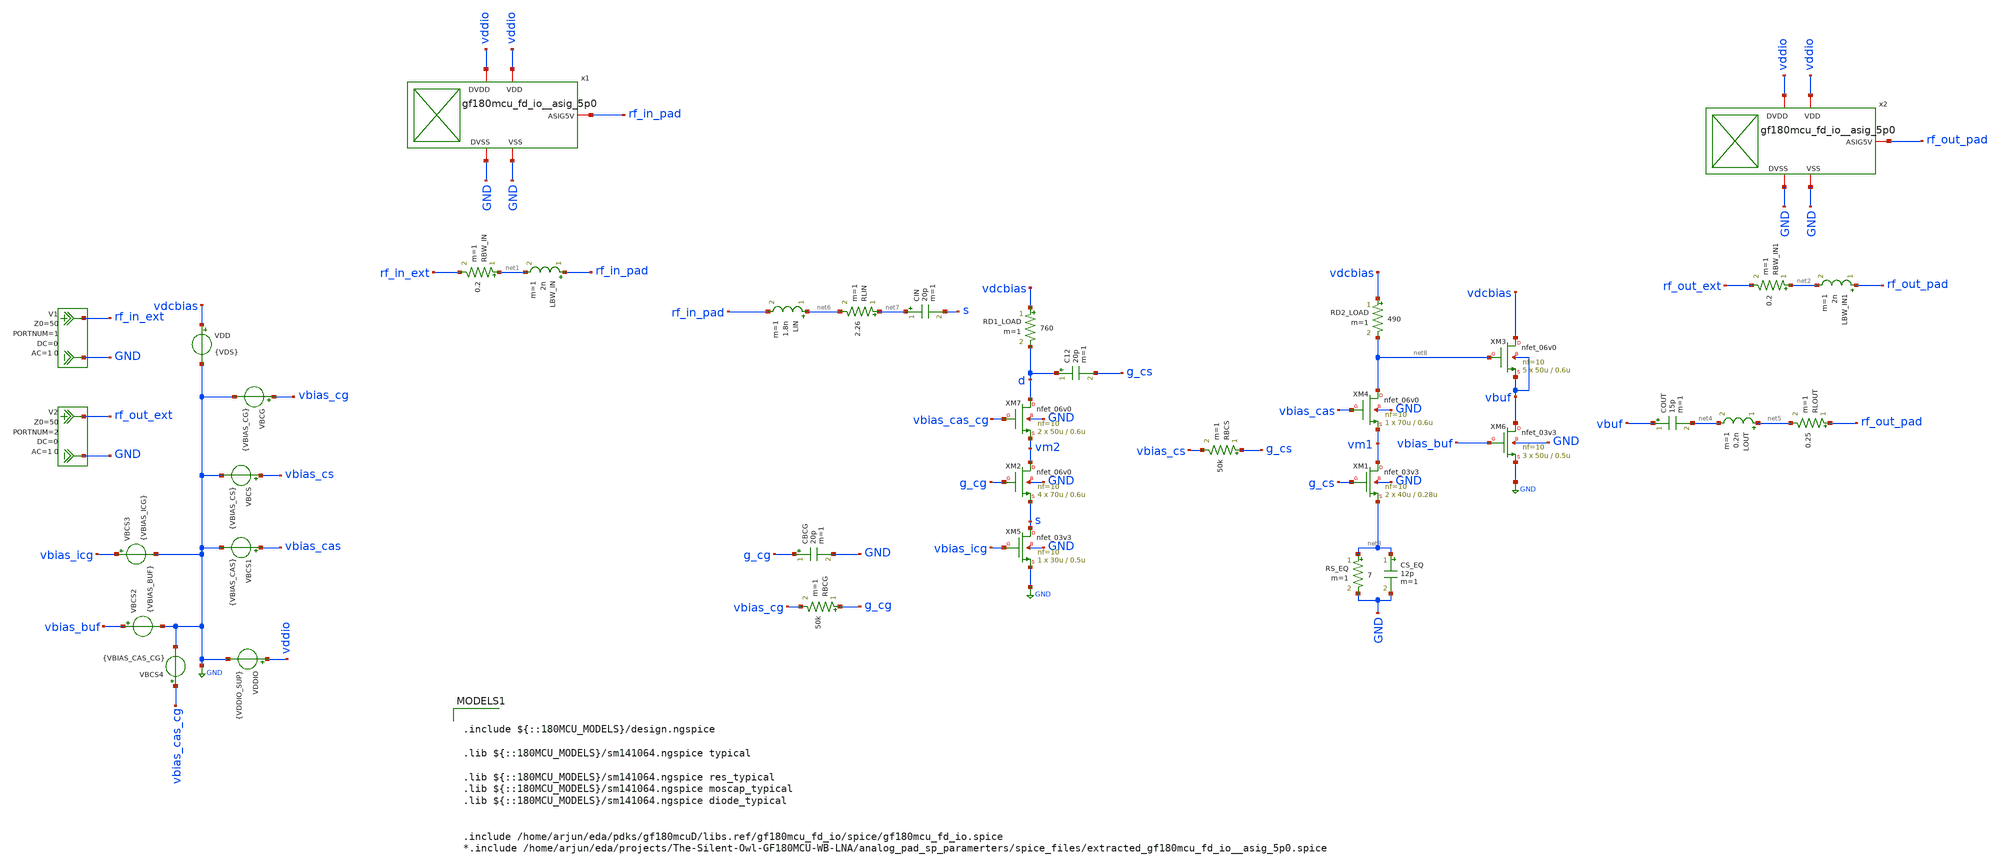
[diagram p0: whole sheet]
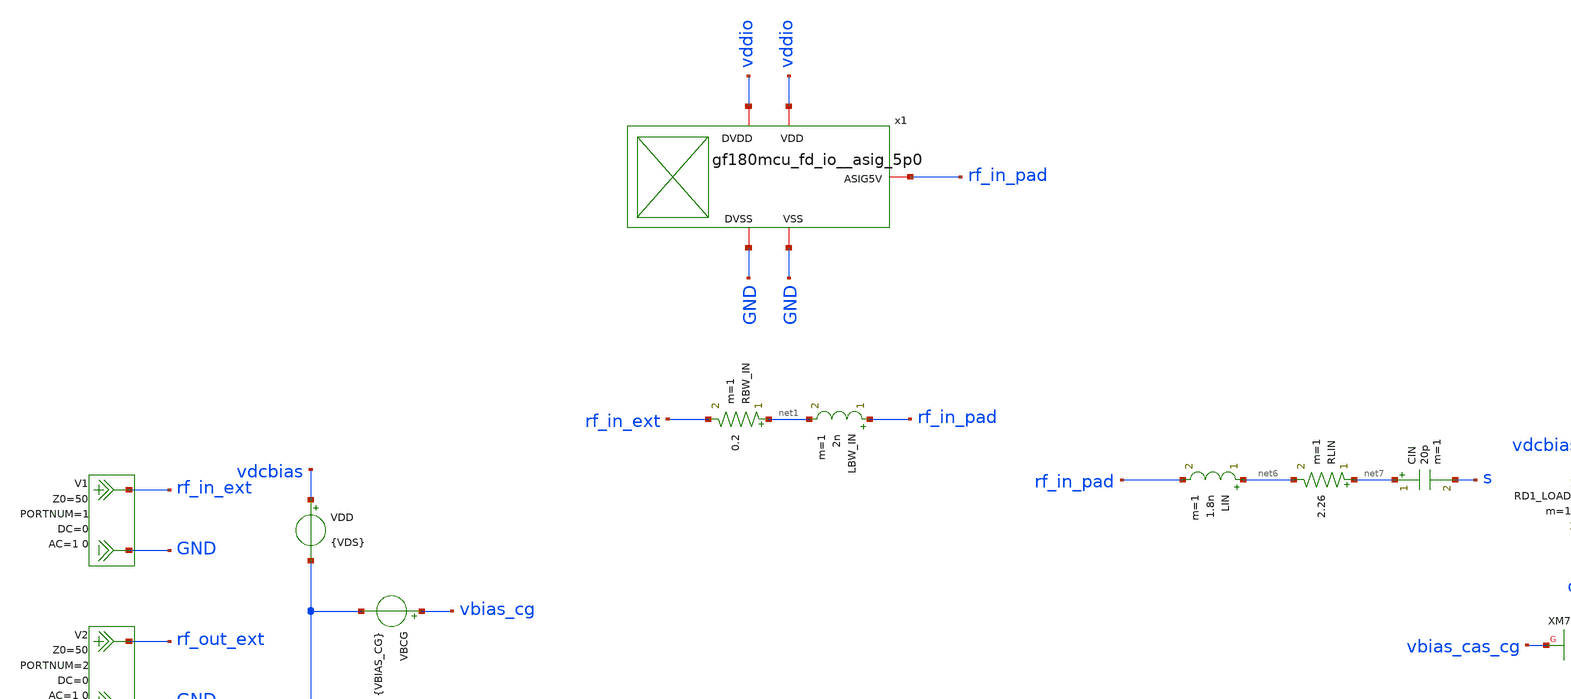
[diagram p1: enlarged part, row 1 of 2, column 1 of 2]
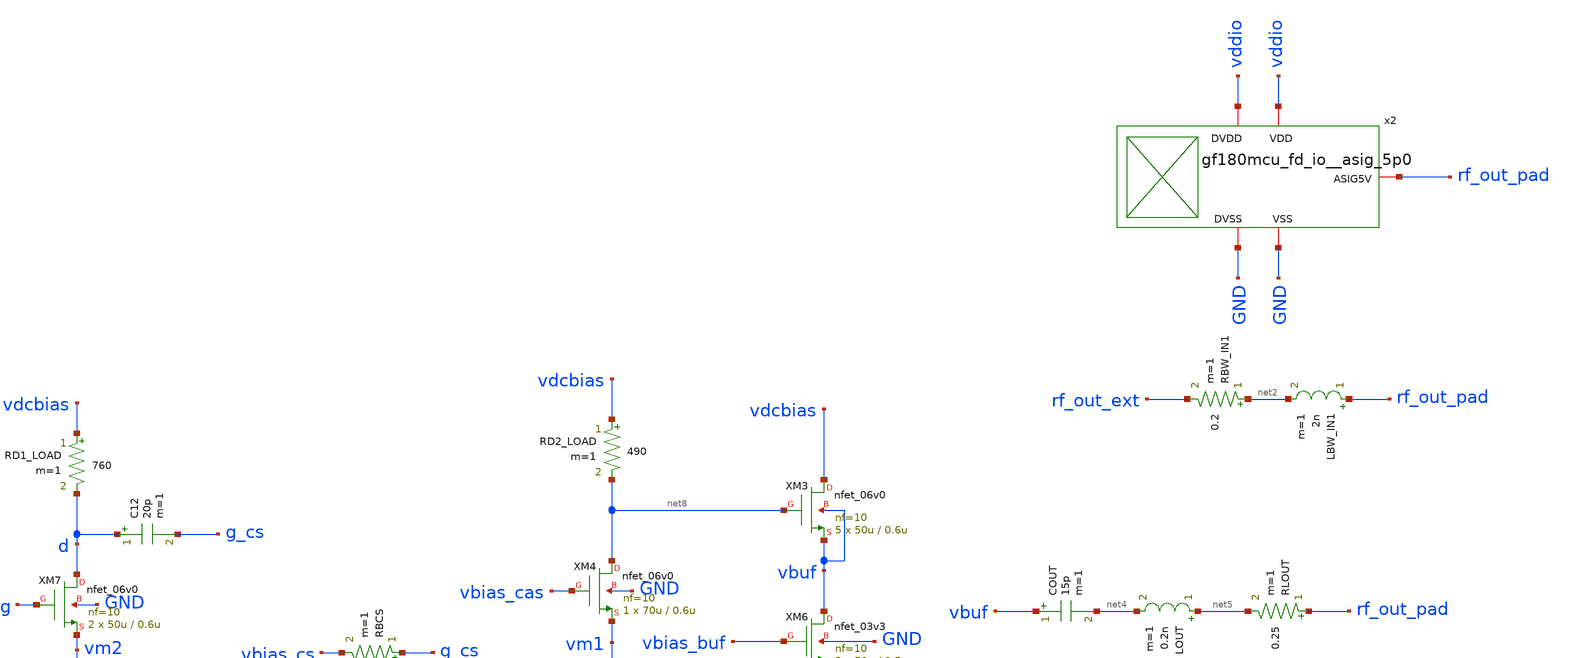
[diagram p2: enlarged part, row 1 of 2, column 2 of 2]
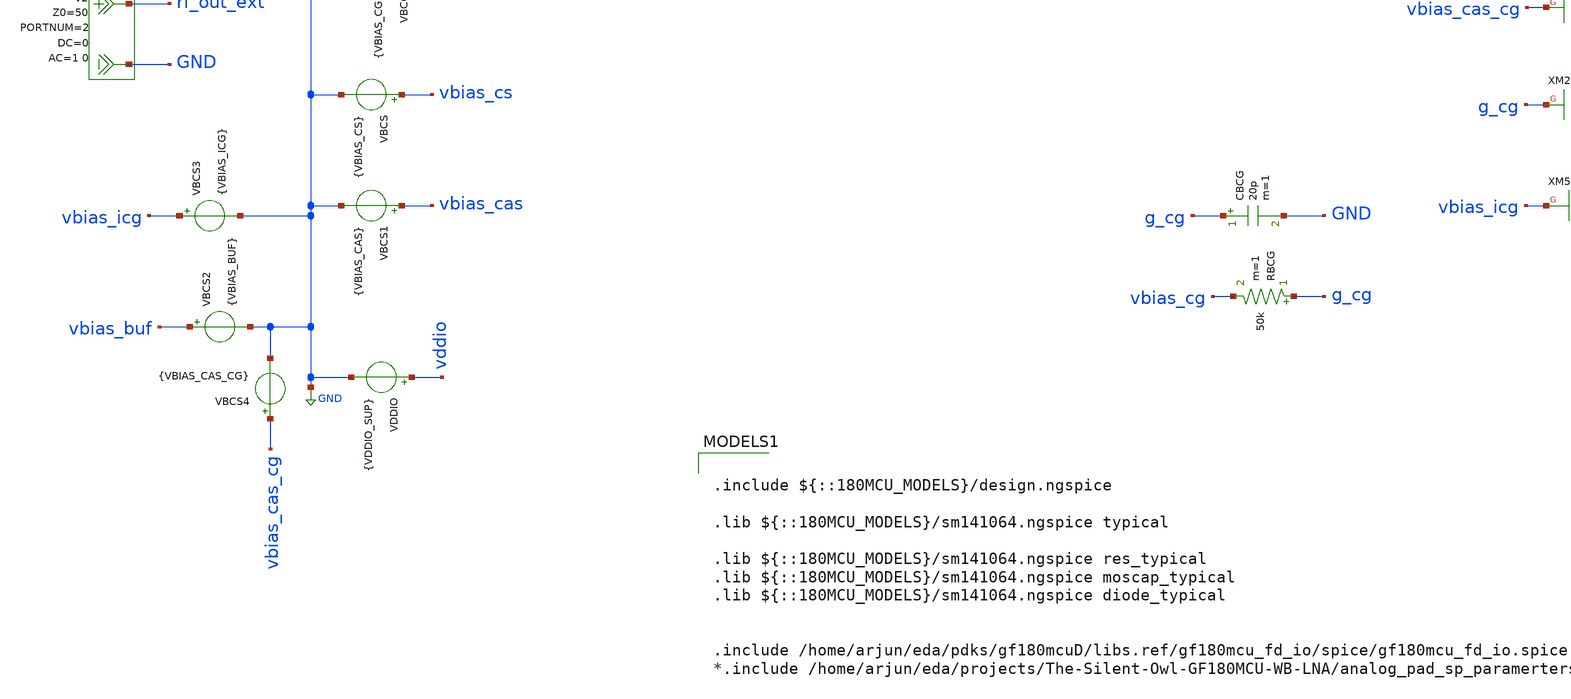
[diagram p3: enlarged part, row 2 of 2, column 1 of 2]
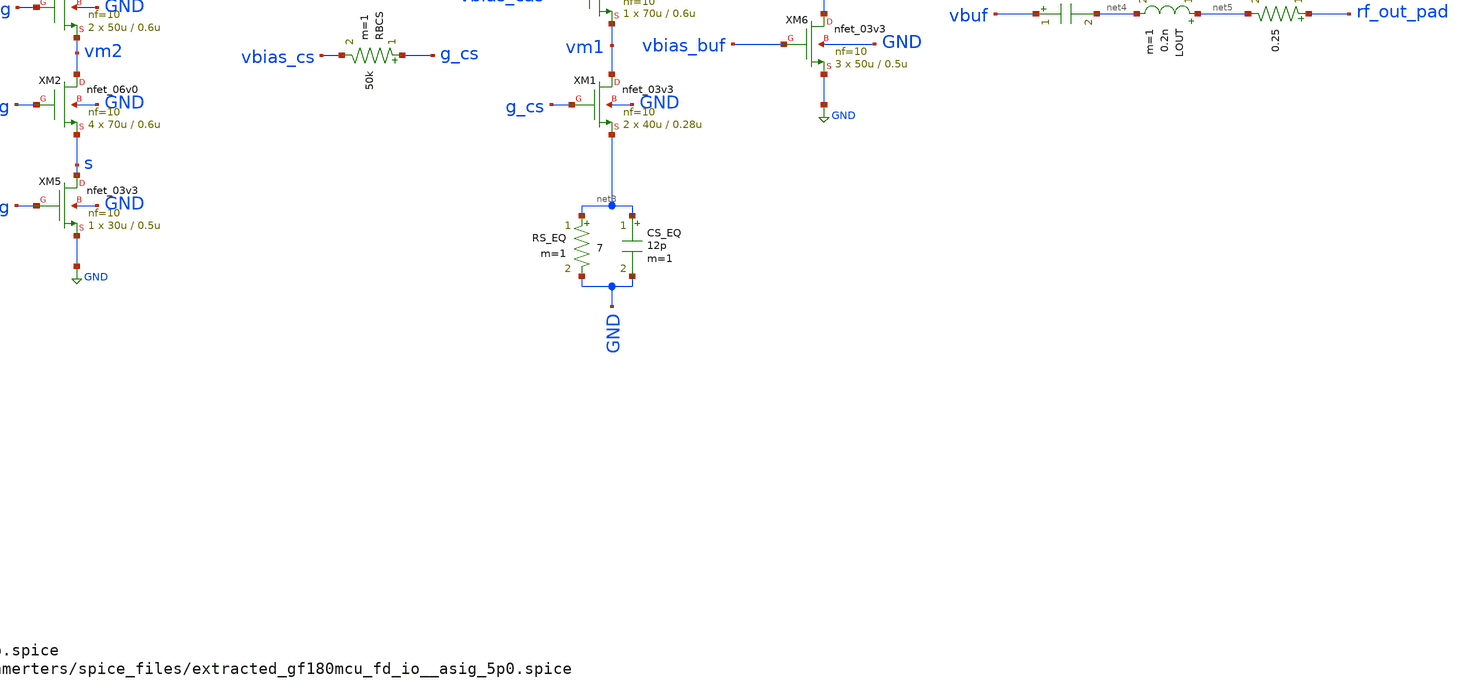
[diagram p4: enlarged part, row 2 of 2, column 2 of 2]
** sch_path: NFmin_Simulation/simulations/lna_core_06V_cgcs_2.sch
**.subckt lna_core_06V_cgcs_2
VBCG vbias_cg GND {VBIAS_CG}
VDD vdcbias GND {VDS}
C12 d g_cs 20p m=1
CIN net7 s 20p m=1
V1 rf_in_ext GND DC 0 AC 1 0 portnum 1 z0 50
V2 rf_out_ext GND DC 0 AC 1 0 portnum 2 z0 50
XM2 vm2 g_cg s GND nfet_06v0 L=0.6u W=70u nf=10 ad='int((nf+1)/2) * W/nf * 0.18u' as='int((nf+2)/2) * W/nf * 0.18u'
+ pd='2*int((nf+1)/2) * (W/nf + 0.18u)' ps='2*int((nf+2)/2) * (W/nf + 0.18u)' nrd='0.18u / W' nrs='0.18u / W'
+ sa=0 sb=0 sd=0 m=4
RBCG g_cg vbias_cg 50k m=1
CBCG g_cg GND 20p m=1
LBW_IN rf_in_pad net1 2n m=1
RBW_IN net1 rf_in_ext 0.2 m=1
VDDIO vddio GND {VDDIO_SUP}
LBW_IN1 rf_out_pad net2 2n m=1
RBW_IN1 net2 rf_out_ext 0.2 m=1
VBCS vbias_cs GND {VBIAS_CS}
RD1_LOAD vdcbias d 760 m=1
RBCS g_cs vbias_cs 50k m=1
RD2_LOAD vdcbias net8 490 m=1
XM3 vdcbias net8 vbuf vbuf nfet_06v0 L=0.6u W=50u nf=10 ad='int((nf+1)/2) * W/nf * 0.18u' as='int((nf+2)/2) * W/nf * 0.18u'
+ pd='2*int((nf+1)/2) * (W/nf + 0.18u)' ps='2*int((nf+2)/2) * (W/nf + 0.18u)' nrd='0.18u / W' nrs='0.18u / W'
+ sa=0 sb=0 sd=0 m=5
COUT vbuf net4 15p m=1
LOUT net5 net4 0.2n m=1
RLOUT rf_out_pad net5 0.25 m=1
LIN net6 rf_in_pad 1.8n m=1
RLIN net7 net6 2.26 m=1
XM4 net8 vbias_cas vm1 GND nfet_06v0 L=0.6u W=70u nf=10 ad='int((nf+1)/2) * W/nf * 0.18u' as='int((nf+2)/2) * W/nf * 0.18u'
+ pd='2*int((nf+1)/2) * (W/nf + 0.18u)' ps='2*int((nf+2)/2) * (W/nf + 0.18u)' nrd='0.18u / W' nrs='0.18u / W'
+ sa=0 sb=0 sd=0 m=1
VBCS1 vbias_cas GND {VBIAS_CAS}
VBCS2 vbias_buf GND {VBIAS_BUF}
VBCS3 vbias_icg GND {VBIAS_ICG}
XM5 s vbias_icg GND GND nfet_03v3 L=0.5u W=30u nf=10 ad='int((nf+1)/2) * W/nf * 0.18u' as='int((nf+2)/2) * W/nf * 0.18u'
+ pd='2*int((nf+1)/2) * (W/nf + 0.18u)' ps='2*int((nf+2)/2) * (W/nf + 0.18u)' nrd='0.18u / W' nrs='0.18u / W'
+ sa=0 sb=0 sd=0 m=1
XM6 vbuf vbias_buf GND GND nfet_03v3 L=0.5u W=50u nf=10 ad='int((nf+1)/2) * W/nf * 0.18u' as='int((nf+2)/2) * W/nf * 0.18u'
+ pd='2*int((nf+1)/2) * (W/nf + 0.18u)' ps='2*int((nf+2)/2) * (W/nf + 0.18u)' nrd='0.18u / W' nrs='0.18u / W'
+ sa=0 sb=0 sd=0 m=3
RS_EQ net3 GND 7 m=1
CS_EQ net3 GND 12p m=1
XM1 vm1 g_cs net3 GND nfet_03v3 L=0.28u W=40u nf=10 ad='int((nf+1)/2) * W/nf * 0.18u' as='int((nf+2)/2) * W/nf * 0.18u'
+ pd='2*int((nf+1)/2) * (W/nf + 0.18u)' ps='2*int((nf+2)/2) * (W/nf + 0.18u)' nrd='0.18u / W' nrs='0.18u / W'
+ sa=0 sb=0 sd=0 m=2
VBCS4 vbias_cas_cg GND {VBIAS_CAS_CG}
XM7 d vbias_cas_cg vm2 GND nfet_06v0 L=0.6u W=50u nf=10 ad='int((nf+1)/2) * W/nf * 0.18u' as='int((nf+2)/2) * W/nf * 0.18u'
+ pd='2*int((nf+1)/2) * (W/nf + 0.18u)' ps='2*int((nf+2)/2) * (W/nf + 0.18u)' nrd='0.18u / W' nrs='0.18u / W'
+ sa=0 sb=0 sd=0 m=2
x1 rf_in_pad vddio GND vddio GND gf180mcu_fd_io__asig_5p0
x2 rf_out_pad vddio GND vddio GND gf180mcu_fd_io__asig_5p0
**** begin user architecture code




* =============================================================================
* FIXED SUPPLY / PACKAGE VALUES
* =============================================================================

.param VDS=5.0
.param VDDIO_SUP=5.0
.param L_BW=2n
.param R_BW=0.2


* =============================================================================
* FIXED INPUT NETWORK
* =============================================================================

.param L_IN=1.80n
.param R_L_IN=1.5
.param CIN_VAL=100p
.param C_SH_IN=1f


* =============================================================================
* FIXED XM2 COMMON-GATE INPUT STAGE
* =============================================================================

.param VBIAS_CG=2.20
.param W_CG=140u
.param M_CG=2
.param L_CG=0.60u
.param RD1=760
.param RBIAS_CG=50k
.param CBYP_CG=20p


* =============================================================================
* FIXED MIXED-VOLTAGE XM1/XM4 STAGE
* =============================================================================

.param C12_VAL=33p

.param VBIAS_CS=0.95
.param W_CS=40u
.param M_CS=2
.param L_CS=0.28u
.param RBIAS_CS=50k

.param VBIAS_CAS=3.30
.param W_CAS=70u
.param M_CAS=1
.param L_CAS=0.60u
.param RD2=490

.param RS_EQ=7
.param CSEQ_VAL=12p


* =============================================================================
* FIXED BODY-TIED SOURCE FOLLOWER
* =============================================================================

.param W_SF=125u
.param M_SF=2
.param L_SF=0.60u
.param RG_SF_VAL=0.01


* =============================================================================
* FIXED OUTPUT NETWORK
* =============================================================================

.param COUT_VAL=56p
.param L_OUT=0.20n
.param R_L_OUT=1.5
.param C_SH_OUT=1f


* =============================================================================
* FIXED XM5 COMMON-GATE CURRENT SINK
* =============================================================================

.param VBIAS_ICG=1.55
.param L_BIAS_CG=0.50u
.param W_BIAS_CG=30u
.param M_BIAS_CG=1


* =============================================================================
* FIXED XM6 SOURCE-FOLLOWER CURRENT SINK
* =============================================================================

.param VBIAS_BUF=2.40
.param L_BIAS_SF=0.50u
.param W_BIAS_SF=50u
.param M_BIAS_SF=3


* =============================================================================
* XM7 CG-CASCODE SWEEP PARAMETERS
* =============================================================================

.param VBIAS_CAS_CG=3.40
.param L_CAS_CG=0.60u
.param W_CAS_CG=50u
.param M_CAS_CG=2

* =============================================================================
* NGSPICE-42 REPORT BLOCK FOR lna_core_06V_cgcs
* Based on the scalar-save and fresh-plot method from the supplied reference.
* No double quote characters are used.
* Replace the existing .control through .endc block with this block.
* =============================================================================

.control

set noaskquit
set wr_singlescale
set wr_vecnames
set numdgt=10

let target_gain_bw=10.0

echo ============================================================ > lna_core_06V_cgcs_report.txt
echo GF180MCU_LNA_CORE_06V_CGCS_DETAILED_REPORT >> lna_core_06V_cgcs_report.txt
echo TARGET_FREQUENCY_HZ 2.400e9 >> lna_core_06V_cgcs_report.txt
echo TARGET_BAND_HZ 2.300e9 2.500e9 >> lna_core_06V_cgcs_report.txt
echo GAIN_BANDWIDTH_THRESHOLD_DB 10.0 >> lna_core_06V_cgcs_report.txt
echo PORT_REFERENCE_OHM 50 >> lna_core_06V_cgcs_report.txt
echo ============================================================ >> lna_core_06V_cgcs_report.txt

* =============================================================================
* DC OPERATING POINT
* =============================================================================

op

let pdcop=1e3*(abs(i(VDD))*v(vdcbias)+abs(i(VDDIO))*v(vddio))
let icoreop=abs(i(VDD))
let iioop=abs(i(VDDIO))

let vsop=v(s)
let vdop=v(d)
let vnet3op=v(net3)
let vnet8op=v(net8)
let vbufop=v(vbuf)
let vgcsop=v(g_cs)
let vgcgop=v(g_cg)

let id1op=abs(@m.xm1.m0[id])
let gm1op=@m.xm1.m0[gm]
let gmb1op=@m.xm1.m0[gmbs]
let gds1op=@m.xm1.m0[gds]
let vgs1op=@m.xm1.m0[vgs]
let vds1op=@m.xm1.m0[vds]
let vbs1op=@m.xm1.m0[vbs]
let vth1op=@m.xm1.m0[vth]
let vov1op=vgs1op-vth1op
let vdsat1op=abs(@m.xm1.m0[vdsat])
let sat1op=vds1op-vdsat1op
let gmid1op=gm1op/(id1op+1e-30)
let ro1op=1/(gds1op+1e-30)

let id2op=abs(@m.xm2.m0[id])
let gm2op=@m.xm2.m0[gm]
let gmb2op=@m.xm2.m0[gmbs]
let gds2op=@m.xm2.m0[gds]
let vgs2op=@m.xm2.m0[vgs]
let vds2op=@m.xm2.m0[vds]
let vbs2op=@m.xm2.m0[vbs]
let vth2op=@m.xm2.m0[vth]
let vov2op=vgs2op-vth2op
let vdsat2op=abs(@m.xm2.m0[vdsat])
let sat2op=vds2op-vdsat2op
let gmid2op=gm2op/(id2op+1e-30)
let ro2op=1/(gds2op+1e-30)

let id3op=abs(@m.xm3.m0[id])
let gm3op=@m.xm3.m0[gm]
let gmb3op=@m.xm3.m0[gmbs]
let gds3op=@m.xm3.m0[gds]
let vgs3op=@m.xm3.m0[vgs]
let vds3op=@m.xm3.m0[vds]
let vbs3op=@m.xm3.m0[vbs]
let vth3op=@m.xm3.m0[vth]
let vov3op=vgs3op-vth3op
let vdsat3op=abs(@m.xm3.m0[vdsat])
let sat3op=vds3op-vdsat3op
let gmid3op=gm3op/(id3op+1e-30)
let ro3op=1/(gds3op+1e-30)

let id4op=abs(@m.xm4.m0[id])
let gm4op=@m.xm4.m0[gm]
let gmb4op=@m.xm4.m0[gmbs]
let gds4op=@m.xm4.m0[gds]
let vgs4op=@m.xm4.m0[vgs]
let vds4op=@m.xm4.m0[vds]
let vbs4op=@m.xm4.m0[vbs]
let vth4op=@m.xm4.m0[vth]
let vov4op=vgs4op-vth4op
let vdsat4op=abs(@m.xm4.m0[vdsat])
let sat4op=vds4op-vdsat4op
let gmid4op=gm4op/(id4op+1e-30)
let ro4op=1/(gds4op+1e-30)

let id5op=abs(@m.xm5.m0[id])
let gm5op=@m.xm5.m0[gm]
let gmb5op=@m.xm5.m0[gmbs]
let gds5op=@m.xm5.m0[gds]
let vgs5op=@m.xm5.m0[vgs]
let vds5op=@m.xm5.m0[vds]
let vbs5op=@m.xm5.m0[vbs]
let vth5op=@m.xm5.m0[vth]
let vov5op=vgs5op-vth5op
let vdsat5op=abs(@m.xm5.m0[vdsat])
let sat5op=vds5op-vdsat5op
let gmid5op=gm5op/(id5op+1e-30)
let ro5op=1/(gds5op+1e-30)

let id6op=abs(@m.xm6.m0[id])
let gm6op=@m.xm6.m0[gm]
let gmb6op=@m.xm6.m0[gmbs]
let gds6op=@m.xm6.m0[gds]
let vgs6op=@m.xm6.m0[vgs]
let vds6op=@m.xm6.m0[vds]
let vbs6op=@m.xm6.m0[vbs]
let vth6op=@m.xm6.m0[vth]
let vov6op=vgs6op-vth6op
let vdsat6op=abs(@m.xm6.m0[vdsat])
let sat6op=vds6op-vdsat6op
let gmid6op=gm6op/(id6op+1e-30)
let ro6op=1/(gds6op+1e-30)

let id7op=abs(@m.xm7.m0[id])
let gm7op=@m.xm7.m0[gm]
let gmb7op=@m.xm7.m0[gmbs]
let gds7op=@m.xm7.m0[gds]
let vgs7op=@m.xm7.m0[vgs]
let vds7op=@m.xm7.m0[vds]
let vbs7op=@m.xm7.m0[vbs]
let vth7op=@m.xm7.m0[vth]
let vov7op=vgs7op-vth7op
let vdsat7op=abs(@m.xm7.m0[vdsat])
let sat7op=vds7op-vdsat7op
let gmid7op=gm7op/(id7op+1e-30)
let ro7op=1/(gds7op+1e-30)

let vnet9op=vnet3op+vds1op
let vnet9check=vnet8op-vds4op
let vnet9diff=vnet9op-vnet9check
let vnet10op=vsop+vds2op
let vnet10check=vdop-vds7op
let vnet10diff=vnet10op-vnet10check

set op_pdc=$&pdcop
set op_icore=$&icoreop
set op_iio=$&iioop
set op_vs=$&vsop
set op_vnet10=$&vnet10op
set op_vnet10check=$&vnet10check
set op_vnet10diff=$&vnet10diff
set op_vd=$&vdop
set op_vnet3=$&vnet3op
set op_vnet9=$&vnet9op
set op_vnet9check=$&vnet9check
set op_vnet9diff=$&vnet9diff
set op_vnet8=$&vnet8op
set op_vbuf=$&vbufop
set op_vgcs=$&vgcsop
set op_vgcg=$&vgcgop

set op_id1=$&id1op
set op_gm1=$&gm1op
set op_gmb1=$&gmb1op
set op_gds1=$&gds1op
set op_vgs1=$&vgs1op
set op_vds1=$&vds1op
set op_vbs1=$&vbs1op
set op_vth1=$&vth1op
set op_vov1=$&vov1op
set op_vdsat1=$&vdsat1op
set op_sat1=$&sat1op
set op_gmid1=$&gmid1op
set op_ro1=$&ro1op

set op_id2=$&id2op
set op_gm2=$&gm2op
set op_gmb2=$&gmb2op
set op_gds2=$&gds2op
set op_vgs2=$&vgs2op
set op_vds2=$&vds2op
set op_vbs2=$&vbs2op
set op_vth2=$&vth2op
set op_vov2=$&vov2op
set op_vdsat2=$&vdsat2op
set op_sat2=$&sat2op
set op_gmid2=$&gmid2op
set op_ro2=$&ro2op

set op_id3=$&id3op
set op_gm3=$&gm3op
set op_gmb3=$&gmb3op
set op_gds3=$&gds3op
set op_vgs3=$&vgs3op
set op_vds3=$&vds3op
set op_vbs3=$&vbs3op
set op_vth3=$&vth3op
set op_vov3=$&vov3op
set op_vdsat3=$&vdsat3op
set op_sat3=$&sat3op
set op_gmid3=$&gmid3op
set op_ro3=$&ro3op

set op_id4=$&id4op
set op_gm4=$&gm4op
set op_gmb4=$&gmb4op
set op_gds4=$&gds4op
set op_vgs4=$&vgs4op
set op_vds4=$&vds4op
set op_vbs4=$&vbs4op
set op_vth4=$&vth4op
set op_vov4=$&vov4op
set op_vdsat4=$&vdsat4op
set op_sat4=$&sat4op
set op_gmid4=$&gmid4op
set op_ro4=$&ro4op

set op_id5=$&id5op
set op_gm5=$&gm5op
set op_gmb5=$&gmb5op
set op_gds5=$&gds5op
set op_vgs5=$&vgs5op
set op_vds5=$&vds5op
set op_vbs5=$&vbs5op
set op_vth5=$&vth5op
set op_vov5=$&vov5op
set op_vdsat5=$&vdsat5op
set op_sat5=$&sat5op
set op_gmid5=$&gmid5op
set op_ro5=$&ro5op

set op_id6=$&id6op
set op_gm6=$&gm6op
set op_gmb6=$&gmb6op
set op_gds6=$&gds6op
set op_vgs6=$&vgs6op
set op_vds6=$&vds6op
set op_vbs6=$&vbs6op
set op_vth6=$&vth6op
set op_vov6=$&vov6op
set op_vdsat6=$&vdsat6op
set op_sat6=$&sat6op
set op_gmid6=$&gmid6op
set op_ro6=$&ro6op

set op_id7=$&id7op
set op_gm7=$&gm7op
set op_gmb7=$&gmb7op
set op_gds7=$&gds7op
set op_vgs7=$&vgs7op
set op_vds7=$&vds7op
set op_vbs7=$&vbs7op
set op_vth7=$&vth7op
set op_vov7=$&vov7op
set op_vdsat7=$&vdsat7op
set op_sat7=$&sat7op
set op_gmid7=$&gmid7op
set op_ro7=$&ro7op

echo ============================================================ >> lna_core_06V_cgcs_report.txt
echo DC_SUPPLY_AND_NODE_VOLTAGES >> lna_core_06V_cgcs_report.txt
echo PDC_mW $op_pdc ICORE_A $op_icore IIO_A $op_iio >> lna_core_06V_cgcs_report.txt
echo NODES_V S $op_vs NET10_DERIVED $op_vnet10 D $op_vd NET3 $op_vnet3 NET9_DERIVED $op_vnet9 NET8
+ $op_vnet8 VBUF $op_vbuf G_CS $op_vgcs G_CG $op_vgcg >> lna_core_06V_cgcs_report.txt
echo HIDDEN_NODE_CHECKS NET10_FROM_XM2 $op_vnet10 NET10_FROM_XM7 $op_vnet10check DIFFERENCE
+ $op_vnet10diff NET9_FROM_XM1 $op_vnet9 NET9_FROM_XM4 $op_vnet9check DIFFERENCE $op_vnet9diff >>
+ lna_core_06V_cgcs_report.txt
echo ============================================================ >> lna_core_06V_cgcs_report.txt
echo TRANSISTOR_OPERATING_POINTS >> lna_core_06V_cgcs_report.txt
echo FIELDS ID_A GM_S GMBS_S GDS_S VGS_V VDS_V VBS_V VTH_V VOV_V VDSAT_V SAT_MARGIN_V
+ GM_OVER_ID_1_PER_V RO_OHM >> lna_core_06V_cgcs_report.txt
echo XM1_CS ID $op_id1 GM $op_gm1 GMBS $op_gmb1 GDS $op_gds1 VGS $op_vgs1 VDS $op_vds1 VBS $op_vbs1
+ VTH $op_vth1 VOV $op_vov1 VDSAT $op_vdsat1 SAT_MARGIN $op_sat1 GMID $op_gmid1 RO $op_ro1 >>
+ lna_core_06V_cgcs_report.txt
echo XM2_CG ID $op_id2 GM $op_gm2 GMBS $op_gmb2 GDS $op_gds2 VGS $op_vgs2 VDS $op_vds2 VBS $op_vbs2
+ VTH $op_vth2 VOV $op_vov2 VDSAT $op_vdsat2 SAT_MARGIN $op_sat2 GMID $op_gmid2 RO $op_ro2 >>
+ lna_core_06V_cgcs_report.txt
echo XM3_SOURCE_FOLLOWER ID $op_id3 GM $op_gm3 GMBS $op_gmb3 GDS $op_gds3 VGS $op_vgs3 VDS $op_vds3
+ VBS $op_vbs3 VTH $op_vth3 VOV $op_vov3 VDSAT $op_vdsat3 SAT_MARGIN $op_sat3 GMID $op_gmid3 RO $op_ro3
+ >> lna_core_06V_cgcs_report.txt
echo XM4_CS_CASCODE ID $op_id4 GM $op_gm4 GMBS $op_gmb4 GDS $op_gds4 VGS $op_vgs4 VDS $op_vds4 VBS
+ $op_vbs4 VTH $op_vth4 VOV $op_vov4 VDSAT $op_vdsat4 SAT_MARGIN $op_sat4 GMID $op_gmid4 RO $op_ro4 >>
+ lna_core_06V_cgcs_report.txt
echo XM5_CG_CURRENT_SINK ID $op_id5 GM $op_gm5 GMBS $op_gmb5 GDS $op_gds5 VGS $op_vgs5 VDS $op_vds5
+ VBS $op_vbs5 VTH $op_vth5 VOV $op_vov5 VDSAT $op_vdsat5 SAT_MARGIN $op_sat5 GMID $op_gmid5 RO $op_ro5
+ >> lna_core_06V_cgcs_report.txt
echo XM6_BUFFER_CURRENT_SINK ID $op_id6 GM $op_gm6 GMBS $op_gmb6 GDS $op_gds6 VGS $op_vgs6 VDS
+ $op_vds6 VBS $op_vbs6 VTH $op_vth6 VOV $op_vov6 VDSAT $op_vdsat6 SAT_MARGIN $op_sat6 GMID $op_gmid6 RO
+ $op_ro6 >> lna_core_06V_cgcs_report.txt
echo XM7_CG_CASCODE ID $op_id7 GM $op_gm7 GMBS $op_gmb7 GDS $op_gds7 VGS $op_vgs7 VDS $op_vds7 VBS
+ $op_vbs7 VTH $op_vth7 VOV $op_vov7 VDSAT $op_vdsat7 SAT_MARGIN $op_sat7 GMID $op_gmid7 RO $op_ro7 >>
+ lna_core_06V_cgcs_report.txt

destroy $curplot

* =============================================================================
* SINGLE BROADBAND RF ANALYSIS
* One reset and one SP run are used for all 1 MHz to 7 GHz RF results.
* Target-band values are extracted from the same dataset.
* This avoids inconsistent port excitation state between repeated SP runs.
* 7000 points from 1 MHz to 7 GHz gives exactly 1 MHz spacing.
* =============================================================================

reset
sp lin 7000 1Meg 7Gig 1
set rfplot=$curplot

let fghz=frequency/1e9

let s11db=db(s_1_1)
let s21db=db(s_2_1)
let s12db=db(s_1_2)
let s22db=db(s_2_2)

let s11re=real(s_1_1)
let s11im=imag(s_1_1)
let s21re=real(s_2_1)
let s21im=imag(s_2_1)
let s12re=real(s_1_2)
let s12im=imag(s_1_2)
let s22re=real(s_2_2)
let s22im=imag(s_2_2)

let nfdb=real(NF)
let nfmin_db=real(NFmin)

let delta=s_1_1*s_2_2-s_1_2*s_2_1
let delta_mag=mag(delta)
let a11=mag(s_1_1)
let a12=mag(s_1_2)
let a21=mag(s_2_1)
let a22=mag(s_2_2)
let mu=(1-a11*a11)/(mag(s_2_2-delta*conj(s_1_1))+mag(s_1_2*s_2_1))
let mup=(1-a22*a22)/(mag(s_1_1-delta*conj(s_2_2))+mag(s_1_2*s_2_1))
let kval=(1-a11*a11-a22*a22+delta_mag*delta_mag)/(2*a12*a21)

let zin=50*(1+s_1_1)/(1-s_1_1)
let zout=50*(1+s_2_2)/(1-s_2_2)
let zin_re=real(zin)
let zin_im=imag(zin)
let zout_re=real(zout)
let zout_im=imag(zout)

let npts=length(frequency)

* Find indices nearest 2.300 GHz, 2.400 GHz and 2.500 GHz.
let ilo=0
let icenter=0
let ihi=0
let errlo=abs(frequency[0]-2.3e9)
let errcenter=abs(frequency[0]-2.4e9)
let errhi=abs(frequency[0]-2.5e9)
let ii=1
while ii < npts
let newerr=abs(frequency[ii]-2.3e9)
if newerr < errlo
let errlo=newerr
let ilo=ii
end
let newerr=abs(frequency[ii]-2.4e9)
if newerr < errcenter
let errcenter=newerr
let icenter=ii
end
let newerr=abs(frequency[ii]-2.5e9)
if newerr < errhi
let errhi=newerr
let ihi=ii
end
let ii=ii+1
end

* Values at the sample nearest 2.400 GHz.
let center_freq=frequency[icenter]
let s11c=s11db[icenter]
let s21c=s21db[icenter]
let s12c=s12db[icenter]
let s22c=s22db[icenter]
let s11rc=s11re[icenter]
let s11ic=s11im[icenter]
let s21rc=s21re[icenter]
let s21ic=s21im[icenter]
let s12rc=s12re[icenter]
let s12ic=s12im[icenter]
let s22rc=s22re[icenter]
let s22ic=s22im[icenter]
let nfc=nfdb[icenter]
let nfminc=nfmin_db[icenter]
let muc=mu[icenter]
let mupc=mup[icenter]
let kc=kval[icenter]
let dmc=delta_mag[icenter]
let zinrc=zin_re[icenter]
let zinic=zin_im[icenter]
let zoutrc=zout_re[icenter]
let zoutic=zout_im[icenter]

* Initialize target-band extrema.
let s11min=s11db[ilo]
let s11max=s11db[ilo]
let s21min=s21db[ilo]
let s21max=s21db[ilo]
let s12min=s12db[ilo]
let s12max=s12db[ilo]
let s22min=s22db[ilo]
let s22max=s22db[ilo]
let nfbandmin=nfdb[ilo]
let nfbandmax=nfdb[ilo]
let nfminbandmin=nfmin_db[ilo]
let nfminbandmax=nfmin_db[ilo]
let mumin=mu[ilo]
let mupmin=mup[ilo]
let kmin=kval[ilo]
let dmax=delta_mag[ilo]

let s11min_i=ilo
let s11max_i=ilo
let s21min_i=ilo
let s21max_i=ilo
let s12min_i=ilo
let s12max_i=ilo
let s22min_i=ilo
let s22max_i=ilo
let nfmin_i=ilo
let nfmax_i=ilo
let nfminpar_min_i=ilo
let nfminpar_max_i=ilo
let mumin_i=ilo
let mupmin_i=ilo
let kmin_i=ilo
let dmax_i=ilo

* Scan 2.300 GHz to 2.500 GHz.
let ii=ilo
while ii <= ihi
if s11db[ii] < s11min
let s11min=s11db[ii]
let s11min_i=ii
end
if s11db[ii] > s11max
let s11max=s11db[ii]
let s11max_i=ii
end
if s21db[ii] < s21min
let s21min=s21db[ii]
let s21min_i=ii
end
if s21db[ii] > s21max
let s21max=s21db[ii]
let s21max_i=ii
end
if s12db[ii] < s12min
let s12min=s12db[ii]
let s12min_i=ii
end
if s12db[ii] > s12max
let s12max=s12db[ii]
let s12max_i=ii
end
if s22db[ii] < s22min
let s22min=s22db[ii]
let s22min_i=ii
end
if s22db[ii] > s22max
let s22max=s22db[ii]
let s22max_i=ii
end
if nfdb[ii] < nfbandmin
let nfbandmin=nfdb[ii]
let nfmin_i=ii
end
if nfdb[ii] > nfbandmax
let nfbandmax=nfdb[ii]
let nfmax_i=ii
end
if nfmin_db[ii] < nfminbandmin
let nfminbandmin=nfmin_db[ii]
let nfminpar_min_i=ii
end
if nfmin_db[ii] > nfminbandmax
let nfminbandmax=nfmin_db[ii]
let nfminpar_max_i=ii
end
if mu[ii] < mumin
let mumin=mu[ii]
let mumin_i=ii
end
if mup[ii] < mupmin
let mupmin=mup[ii]
let mupmin_i=ii
end
if kval[ii] < kmin
let kmin=kval[ii]
let kmin_i=ii
end
if delta_mag[ii] > dmax
let dmax=delta_mag[ii]
let dmax_i=ii
end
let ii=ii+1
end

let gain_ripple=s21max-s21min

let s11min_f=frequency[s11min_i]
let s11max_f=frequency[s11max_i]
let s21min_f=frequency[s21min_i]
let s21max_f=frequency[s21max_i]
let s12min_f=frequency[s12min_i]
let s12max_f=frequency[s12max_i]
let s22min_f=frequency[s22min_i]
let s22max_f=frequency[s22max_i]
let nfmin_f=frequency[nfmin_i]
let nfmax_f=frequency[nfmax_i]
let nfminpar_min_f=frequency[nfminpar_min_i]
let nfminpar_max_f=frequency[nfminpar_max_i]
let mumin_f=frequency[mumin_i]
let mupmin_f=frequency[mupmin_i]
let kmin_f=frequency[kmin_i]
let dmax_f=frequency[dmax_i]

* Find the broadband S21 peak and its index.
let imax=0
let gainmax=s21db[0]
let ii=1
while ii < npts
if s21db[ii] > gainmax
let gainmax=s21db[ii]
let imax=ii
end
let ii=ii+1
end
let peakfreq=frequency[imax]

echo ============================================================ >> lna_core_06V_cgcs_report.txt
echo RF_AT_2P400_GHZ_FROM_SINGLE_BROADBAND_SWEEP >> lna_core_06V_cgcs_report.txt
echo ACTUAL_SAMPLE_HZ $&center_freq >> lna_core_06V_cgcs_report.txt
echo S11_DB $&s11c REAL $&s11rc IMAG $&s11ic >> lna_core_06V_cgcs_report.txt
echo S21_DB $&s21c REAL $&s21rc IMAG $&s21ic >> lna_core_06V_cgcs_report.txt
echo S12_DB $&s12c REAL $&s12rc IMAG $&s12ic >> lna_core_06V_cgcs_report.txt
echo S22_DB $&s22c REAL $&s22rc IMAG $&s22ic >> lna_core_06V_cgcs_report.txt
echo NF_DB $&nfc NFMIN_DB $&nfminc >> lna_core_06V_cgcs_report.txt
echo MU $&muc MUP $&mupc K $&kc DELTA_MAG $&dmc >> lna_core_06V_cgcs_report.txt
echo ZIN_OHM RE $&zinrc IM $&zinic >> lna_core_06V_cgcs_report.txt
echo ZOUT_OHM RE $&zoutrc IM $&zoutic >> lna_core_06V_cgcs_report.txt

echo ============================================================ >> lna_core_06V_cgcs_report.txt
echo RF_MIN_MAX_FROM_2P300_TO_2P500_GHZ >> lna_core_06V_cgcs_report.txt
echo S11_MIN_DB $&s11min AT_HZ $&s11min_f S11_MAX_DB $&s11max AT_HZ $&s11max_f >>
+ lna_core_06V_cgcs_report.txt
echo S21_MIN_DB $&s21min AT_HZ $&s21min_f S21_MAX_DB $&s21max AT_HZ $&s21max_f GAIN_RIPPLE_DB
+ $&gain_ripple >> lna_core_06V_cgcs_report.txt
echo S12_MIN_DB $&s12min AT_HZ $&s12min_f S12_MAX_DB $&s12max AT_HZ $&s12max_f >>
+ lna_core_06V_cgcs_report.txt
echo S22_MIN_DB $&s22min AT_HZ $&s22min_f S22_MAX_DB $&s22max AT_HZ $&s22max_f >>
+ lna_core_06V_cgcs_report.txt
echo NF_MIN_DB $&nfbandmin AT_HZ $&nfmin_f NF_MAX_DB $&nfbandmax AT_HZ $&nfmax_f >>
+ lna_core_06V_cgcs_report.txt
echo NFMIN_PARAMETER_MIN_DB $&nfminbandmin AT_HZ $&nfminpar_min_f NFMIN_PARAMETER_MAX_DB
+ $&nfminbandmax AT_HZ $&nfminpar_max_f >> lna_core_06V_cgcs_report.txt
echo MU_MIN $&mumin AT_HZ $&mumin_f MUP_MIN $&mupmin AT_HZ $&mupmin_f >>
+ lna_core_06V_cgcs_report.txt
echo K_MIN $&kmin AT_HZ $&kmin_f DELTA_MAX $&dmax AT_HZ $&dmax_f >> lna_core_06V_cgcs_report.txt

echo ============================================================ >> lna_core_06V_cgcs_report.txt
echo BROADBAND_GAIN_CHECK_1MHZ_TO_7GHZ >> lna_core_06V_cgcs_report.txt
echo GAIN_AT_2P4_DB $&s21c >> lna_core_06V_cgcs_report.txt
echo BROADBAND_PEAK_HZ $&peakfreq PEAK_GAIN_DB $&gainmax >> lna_core_06V_cgcs_report.txt

echo ============================================================ >> lna_core_06V_cgcs_report.txt
echo TARGET_CENTERED_S21_GE_10DB_BAND >> lna_core_06V_cgcs_report.txt
if s21c >= 10.0
let bwlo=icenter
let bwhi=icenter
let search=1
while search = 1
if bwlo > 0
if s21db[bwlo-1] >= 10.0
let bwlo=bwlo-1
else
let search=0
end
else
let search=0
end
end
let search=1
while search = 1
if bwhi < npts-1
if s21db[bwhi+1] >= 10.0
let bwhi=bwhi+1
else
let search=0
end
else
let search=0
end
end
let bwflo=frequency[bwlo]
let bwfhi=frequency[bwhi]
let bwval=bwfhi-bwflo
let bwcenter=0.5*(bwfhi+bwflo)
let bwfbw=100*bwval/(bwcenter+1e-30)
echo LOWER_HZ $&bwflo UPPER_HZ $&bwfhi BANDWIDTH_HZ $&bwval BAND_CENTER_HZ $&bwcenter
+ FRACTIONAL_BW_PERCENT $&bwfbw >> lna_core_06V_cgcs_report.txt
else
echo NO_VALID_TARGET_CENTERED_BAND S21_AT_2P4_DB $&s21c >> lna_core_06V_cgcs_report.txt
end

echo ============================================================ >> lna_core_06V_cgcs_report.txt
echo GLOBAL_CONTIGUOUS_S21_GE_10DB_BAND_AROUND_PEAK >> lna_core_06V_cgcs_report.txt
if gainmax >= 10.0
let bwlo=imax
let bwhi=imax
let search=1
while search = 1
if bwlo > 0
if s21db[bwlo-1] >= 10.0
let bwlo=bwlo-1
else
let search=0
end
else
let search=0
end
end
let search=1
while search = 1
if bwhi < npts-1
if s21db[bwhi+1] >= 10.0
let bwhi=bwhi+1
else
let search=0
end
else
let search=0
end
end
let bwflo=frequency[bwlo]
let bwfhi=frequency[bwhi]
let bwval=bwfhi-bwflo
let bwcenter=0.5*(bwfhi+bwflo)
let bwfbw=100*bwval/(bwcenter+1e-30)
echo LOWER_HZ $&bwflo UPPER_HZ $&bwfhi BANDWIDTH_HZ $&bwval BAND_CENTER_HZ $&bwcenter
+ FRACTIONAL_BW_PERCENT $&bwfbw >> lna_core_06V_cgcs_report.txt
else
echo NO_S21_ABOVE_10DB_FROM_1MHZ_TO_7GHZ PEAK_GAIN_DB $&gainmax PEAK_FREQUENCY_HZ $&peakfreq >>
+ lna_core_06V_cgcs_report.txt
end

wrdata lna_core_06V_cgcs_target_band.dat frequency s_1_1 s_2_1 s_1_2 s_2_2 s11db s21db s12db s22db
+ nfdb nfmin_db kval mu mup delta_mag zin_re zin_im zout_re zout_im
wrdata lna_core_06V_cgcs_broadband.dat frequency s11db s21db s12db s22db nfdb nfmin_db kval mu mup
+ delta_mag zin_re zin_im zout_re zout_im

* =============================================================================
* WIDEBAND STABILITY 10 MHZ TO 30 GHZ
* =============================================================================

sp dec 101 10Meg 30G 1
set stabilityplot=$curplot

let wbdelta=s_1_1*s_2_2-s_1_2*s_2_1
let wbmd=mag(wbdelta)
let wba11=mag(s_1_1)
let wba12=mag(s_1_2)
let wba21=mag(s_2_1)
let wba22=mag(s_2_2)
let wbmu=(1-wba11*wba11)/(mag(s_2_2-wbdelta*conj(s_1_1))+mag(s_1_2*s_2_1))
let wbmup=(1-wba22*wba22)/(mag(s_1_1-wbdelta*conj(s_2_2))+mag(s_1_2*s_2_1))
let wbk=(1-wba11*wba11-wba22*wba22+wbmd*wbmd)/(2*wba12*wba21)

let wbkmin=minimum(wbk)
let wbmumin=minimum(wbmu)
let wbmupmin=minimum(wbmup)
let wbdmax=maximum(wbmd)

set final_wbkmin=$&wbkmin
set final_wbmumin=$&wbmumin
set final_wbmupmin=$&wbmupmin
set final_wbdmax=$&wbdmax

echo ============================================================ >> lna_core_06V_cgcs_report.txt
echo WIDEBAND_STABILITY_10MHZ_TO_30GHZ >> lna_core_06V_cgcs_report.txt
echo K_MIN $final_wbkmin MU_MIN $final_wbmumin MUP_MIN $final_wbmupmin DELTA_MAX $final_wbdmax >>
+ lna_core_06V_cgcs_report.txt

wrdata lna_core_06V_cgcs_stability.dat frequency wbk wbmu wbmup wbmd

let wbfghz=frequency/1e9

echo ============================================================ >> lna_core_06V_cgcs_report.txt
echo OUTPUT_FILES >> lna_core_06V_cgcs_report.txt
echo REPORT lna_core_06V_cgcs_report.txt >> lna_core_06V_cgcs_report.txt
echo TARGET_DATA lna_core_06V_cgcs_target_band.dat >> lna_core_06V_cgcs_report.txt
echo BROADBAND_DATA lna_core_06V_cgcs_broadband.dat >> lna_core_06V_cgcs_report.txt
echo STABILITY_DATA lna_core_06V_cgcs_stability.dat >> lna_core_06V_cgcs_report.txt
echo PLOTS S11_S21_S12_S22_SEPARATE NF_AND_NFMIN_TOGETHER STABILITY_AND_IMPEDANCE_DIAGNOSTICS >>
+ lna_core_06V_cgcs_report.txt
echo ============================================================ >> lna_core_06V_cgcs_report.txt



* =============================================================================
* VISIBLE PLOTS
* Plot commands are intentionally placed at the very end.
* Neither rfplot nor stabilityplot is destroyed or reset afterward.
* =============================================================================

setplot $rfplot
setscale fghz

* Target band 2.3 GHz to 2.5 GHz
plot s11db xlimit 2.3 2.5
plot s21db xlimit 2.3 2.5
plot s12db xlimit 2.3 2.5
plot s22db xlimit 2.3 2.5
plot nfdb nfmin_db xlimit 2.3 2.5
plot mu mup xlimit 2.3 2.5
plot kval xlimit 2.3 2.5
plot delta_mag xlimit 2.3 2.5
plot zin_re zin_im xlimit 2.3 2.5
plot zout_re zout_im xlimit 2.3 2.5

* Broadband 1 MHz to 7 GHz
plot s11db xlimit 0 7
plot s21db xlimit 0 7
plot s12db xlimit 0 7
plot s22db xlimit 0 7
plot nfdb nfmin_db xlimit 0 7
plot mu mup xlimit 0 7
plot kval xlimit 0 7
plot delta_mag xlimit 0 7
plot zin_re zin_im xlimit 0 7
plot zout_re zout_im xlimit 0 7

* Wideband stability 10 MHz to 30 GHz
setplot $stabilityplot
setscale wbfghz
plot wbmu wbmup
plot wbk
plot wbmd

.endc




.include ${::180MCU_MODELS}/design.ngspice

.lib ${::180MCU_MODELS}/sm141064.ngspice typical

.lib ${::180MCU_MODELS}/sm141064.ngspice res_typical
.lib ${::180MCU_MODELS}/sm141064.ngspice moscap_typical
.lib ${::180MCU_MODELS}/sm141064.ngspice diode_typical


.include /home/arjun/eda/pdks/gf180mcuD/libs.ref/gf180mcu_fd_io/spice/gf180mcu_fd_io.spice
*.include /home/arjun/eda/projects/The-Silent-Owl-GF180MCU-WB-LNA/analog_pad_sp_paramerters/spice_files/extracted_gf180mcu_fd_io__asig_5p0.spice

**** end user architecture code
**.ends
.GLOBAL GND
.end
